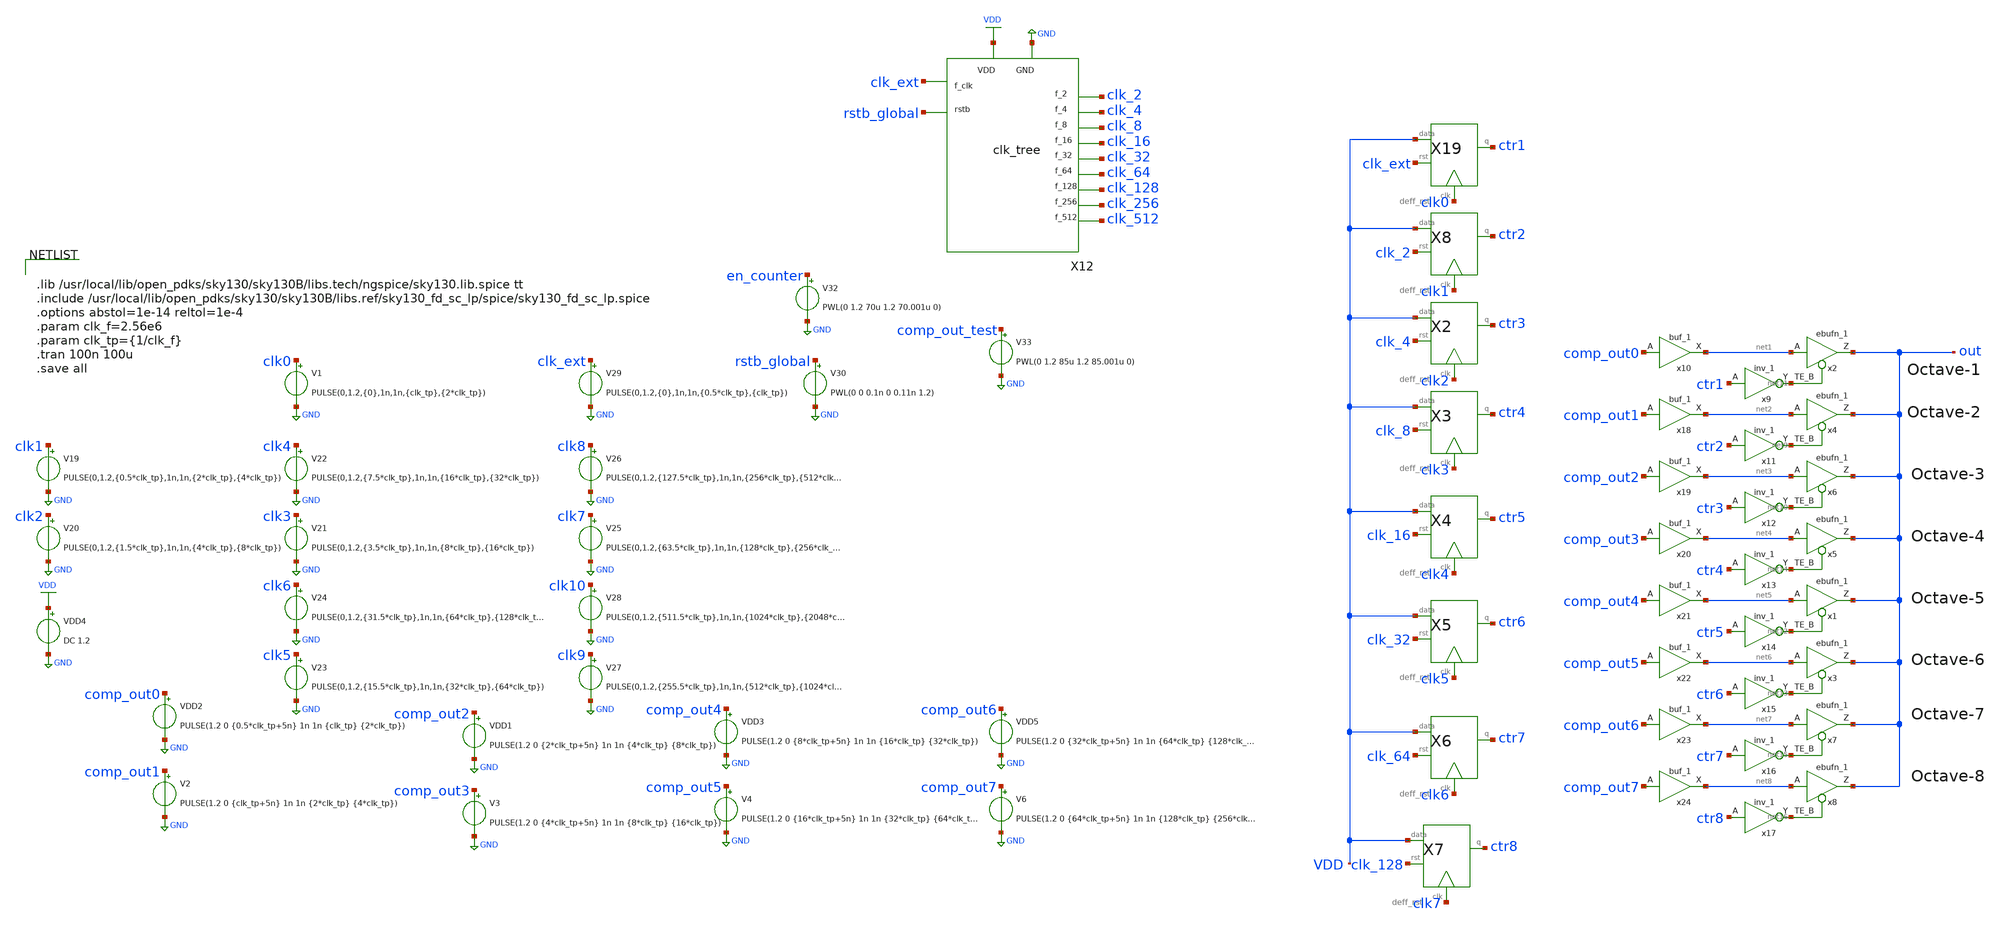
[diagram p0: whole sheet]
** sch_path: xschem/readout/readout_final.sch
**.subckt readout_final
x4 net2 net9 GND GND VDD VDD out sky130_fd_sc_lp__ebufn_1
x6 net3 net10 GND GND VDD VDD out sky130_fd_sc_lp__ebufn_1
x2 net1 net11 GND GND VDD VDD out sky130_fd_sc_lp__ebufn_1
x1 net5 net12 GND GND VDD VDD out sky130_fd_sc_lp__ebufn_1
x3 net6 net13 GND GND VDD VDD out sky130_fd_sc_lp__ebufn_1
x5 net4 net14 GND GND VDD VDD out sky130_fd_sc_lp__ebufn_1
x7 net7 net15 GND GND VDD VDD out sky130_fd_sc_lp__ebufn_1
x8 net8 net16 GND GND VDD VDD out sky130_fd_sc_lp__ebufn_1
X12 rstb_global clk_ext clk_2 clk_4 clk_8 clk_16 clk_32 clk_64 clk_128 clk_256 clk_512 VDD GND
+ clk_tree
X8 VDD clk1 ctr2 clk_2 deff_rst
X19 VDD clk0 ctr1 clk_ext deff_rst
x9 ctr1 GND GND VDD VDD net11 sky130_fd_sc_lp__inv_1
X2 VDD clk2 ctr3 clk_4 deff_rst
X3 VDD clk3 ctr4 clk_8 deff_rst
X4 VDD clk4 ctr5 clk_16 deff_rst
X5 VDD clk5 ctr6 clk_32 deff_rst
X6 VDD clk6 ctr7 clk_64 deff_rst
X7 VDD clk7 ctr8 clk_128 deff_rst
x11 ctr2 GND GND VDD VDD net9 sky130_fd_sc_lp__inv_1
x12 ctr3 GND GND VDD VDD net10 sky130_fd_sc_lp__inv_1
x13 ctr4 GND GND VDD VDD net14 sky130_fd_sc_lp__inv_1
x14 ctr5 GND GND VDD VDD net12 sky130_fd_sc_lp__inv_1
x15 ctr6 GND GND VDD VDD net13 sky130_fd_sc_lp__inv_1
x16 ctr7 GND GND VDD VDD net15 sky130_fd_sc_lp__inv_1
x17 ctr8 GND GND VDD VDD net16 sky130_fd_sc_lp__inv_1
V19 clk1 GND PULSE(0,1.2,{0.5*clk_tp},1n,1n,{2*clk_tp},{4*clk_tp})
VDD4 VDD GND DC 1.2
V20 clk2 GND PULSE(0,1.2,{1.5*clk_tp},1n,1n,{4*clk_tp},{8*clk_tp})
V21 clk3 GND PULSE(0,1.2,{3.5*clk_tp},1n,1n,{8*clk_tp},{16*clk_tp})
V22 clk4 GND PULSE(0,1.2,{7.5*clk_tp},1n,1n,{16*clk_tp},{32*clk_tp})
V23 clk5 GND PULSE(0,1.2,{15.5*clk_tp},1n,1n,{32*clk_tp},{64*clk_tp})
V24 clk6 GND PULSE(0,1.2,{31.5*clk_tp},1n,1n,{64*clk_tp},{128*clk_tp})
V25 clk7 GND PULSE(0,1.2,{63.5*clk_tp},1n,1n,{128*clk_tp},{256*clk_tp})
V26 clk8 GND PULSE(0,1.2,{127.5*clk_tp},1n,1n,{256*clk_tp},{512*clk_tp})
V27 clk9 GND PULSE(0,1.2,{255.5*clk_tp},1n,1n,{512*clk_tp},{1024*clk_tp})
V28 clk10 GND PULSE(0,1.2,{511.5*clk_tp},1n,1n,{1024*clk_tp},{2048*clk_tp})
VDD2 comp_out0 GND PULSE(1.2 0 {0.5*clk_tp+5n} 1n 1n {clk_tp} {2*clk_tp})
V29 clk_ext GND PULSE(0,1.2,{0},1n,1n,{0.5*clk_tp},{clk_tp})
V30 rstb_global GND PWL(0 0 0.1n 0 0.11n 1.2)
V32 en_counter GND PWL(0 1.2 70u 1.2 70.001u 0)
V33 comp_out_test GND PWL(0 1.2 85u 1.2 85.001u 0)
V1 clk0 GND PULSE(0,1.2,{0},1n,1n,{clk_tp},{2*clk_tp})
V2 comp_out1 GND PULSE(1.2 0 {clk_tp+5n} 1n 1n {2*clk_tp} {4*clk_tp})
VDD1 comp_out2 GND PULSE(1.2 0 {2*clk_tp+5n} 1n 1n {4*clk_tp} {8*clk_tp})
V3 comp_out3 GND PULSE(1.2 0 {4*clk_tp+5n} 1n 1n {8*clk_tp} {16*clk_tp})
VDD3 comp_out4 GND PULSE(1.2 0 {8*clk_tp+5n} 1n 1n {16*clk_tp} {32*clk_tp})
V4 comp_out5 GND PULSE(1.2 0 {16*clk_tp+5n} 1n 1n {32*clk_tp} {64*clk_tp})
VDD5 comp_out6 GND PULSE(1.2 0 {32*clk_tp+5n} 1n 1n {64*clk_tp} {128*clk_tp})
V6 comp_out7 GND PULSE(1.2 0 {64*clk_tp+5n} 1n 1n {128*clk_tp} {256*clk_tp})
x10 comp_out0 GND GND VDD VDD net1 sky130_fd_sc_lp__buf_1
x18 comp_out1 GND GND VDD VDD net2 sky130_fd_sc_lp__buf_1
x19 comp_out2 GND GND VDD VDD net3 sky130_fd_sc_lp__buf_1
x20 comp_out3 GND GND VDD VDD net4 sky130_fd_sc_lp__buf_1
x21 comp_out4 GND GND VDD VDD net5 sky130_fd_sc_lp__buf_1
x22 comp_out5 GND GND VDD VDD net6 sky130_fd_sc_lp__buf_1
x23 comp_out6 GND GND VDD VDD net7 sky130_fd_sc_lp__buf_1
x24 comp_out7 GND GND VDD VDD net8 sky130_fd_sc_lp__buf_1
**** begin user architecture code


.lib /usr/local/lib/open_pdks/sky130/sky130B/libs.tech/ngspice/sky130.lib.spice tt
.include /usr/local/lib/open_pdks/sky130/sky130B/libs.ref/sky130_fd_sc_lp/spice/sky130_fd_sc_lp.spice
.options abstol=1e-14 reltol=1e-4
.param clk_f=2.56e6
.param clk_tp={1/clk_f}
.tran 100n 100u
.save all


**** end user architecture code
**.ends

* expanding   symbol:  clk_tree/clk_tree.sym # of pins=13
** sym_path: clk_tree/clk_tree.sym
** sch_path: clk_tree/clk_tree.sch
.subckt clk_tree rstb f_clk f_2 f_4 f_8 f_16 f_32 f_64 f_128 f_256 f_512 VDD GND
*.ipin rstb
*.iopin VDD
*.iopin GND
*.opin f_2
*.opin f_4
*.opin f_8
*.opin f_16
*.opin f_32
*.opin f_64
*.opin f_128
*.opin f_256
*.opin f_512
*.ipin f_clk
x2 f_clk net1 rstb gnd gnd vdd vdd f_2 net1 sky130_fd_sc_lp__dfrbp_1
x4 f_2 net2 rstb gnd gnd vdd vdd f_4 net2 sky130_fd_sc_lp__dfrbp_1
x1 f_4 net3 rstb gnd gnd vdd vdd f_8 net3 sky130_fd_sc_lp__dfrbp_1
x6 f_8 net4 rstb gnd gnd vdd vdd f_16 net4 sky130_fd_sc_lp__dfrbp_1
x7 f_16 net5 rstb gnd gnd vdd vdd f_32 net5 sky130_fd_sc_lp__dfrbp_1
x8 f_32 net6 rstb gnd gnd vdd vdd f_64 net6 sky130_fd_sc_lp__dfrbp_1
x9 f_64 net7 rstb gnd gnd vdd vdd f_128 net7 sky130_fd_sc_lp__dfrbp_1
x14 f_128 net8 rstb gnd gnd vdd vdd f_256 net8 sky130_fd_sc_lp__dfrbp_1
x15 f_256 net9 rstb gnd gnd vdd vdd f_512 net9 sky130_fd_sc_lp__dfrbp_1
.ends


* expanding   symbol:  tryandtest/deff_rst.sym # of pins=4
** sym_path: xschem/tryandtest/deff_rst.sym
** sch_path: xschem/tryandtest/deff_rst.sch
.subckt deff_rst data clk q rst
*.ipin clk
*.ipin data
*.opin q
*.ipin rst
x3 net2 net3 clk GND GND VDD VDD q sky130_fd_sc_lp__mux2_1
x21 net1 data rst GND GND VDD VDD net2 sky130_fd_sc_lp__dfrtn_1
x2 net4 GND GND VDD VDD net1 sky130_fd_sc_lp__inv_1
x5 net5 GND GND VDD VDD net4 sky130_fd_sc_lp__inv_1
x1 net1 data rst GND GND VDD VDD net3 sky130_fd_sc_lp__dfrtp_1
x4 net6 GND GND VDD VDD net5 sky130_fd_sc_lp__inv_1
x6 clk GND GND VDD VDD net6 sky130_fd_sc_lp__inv_1
.ends

.GLOBAL VDD
.GLOBAL GND
.end
